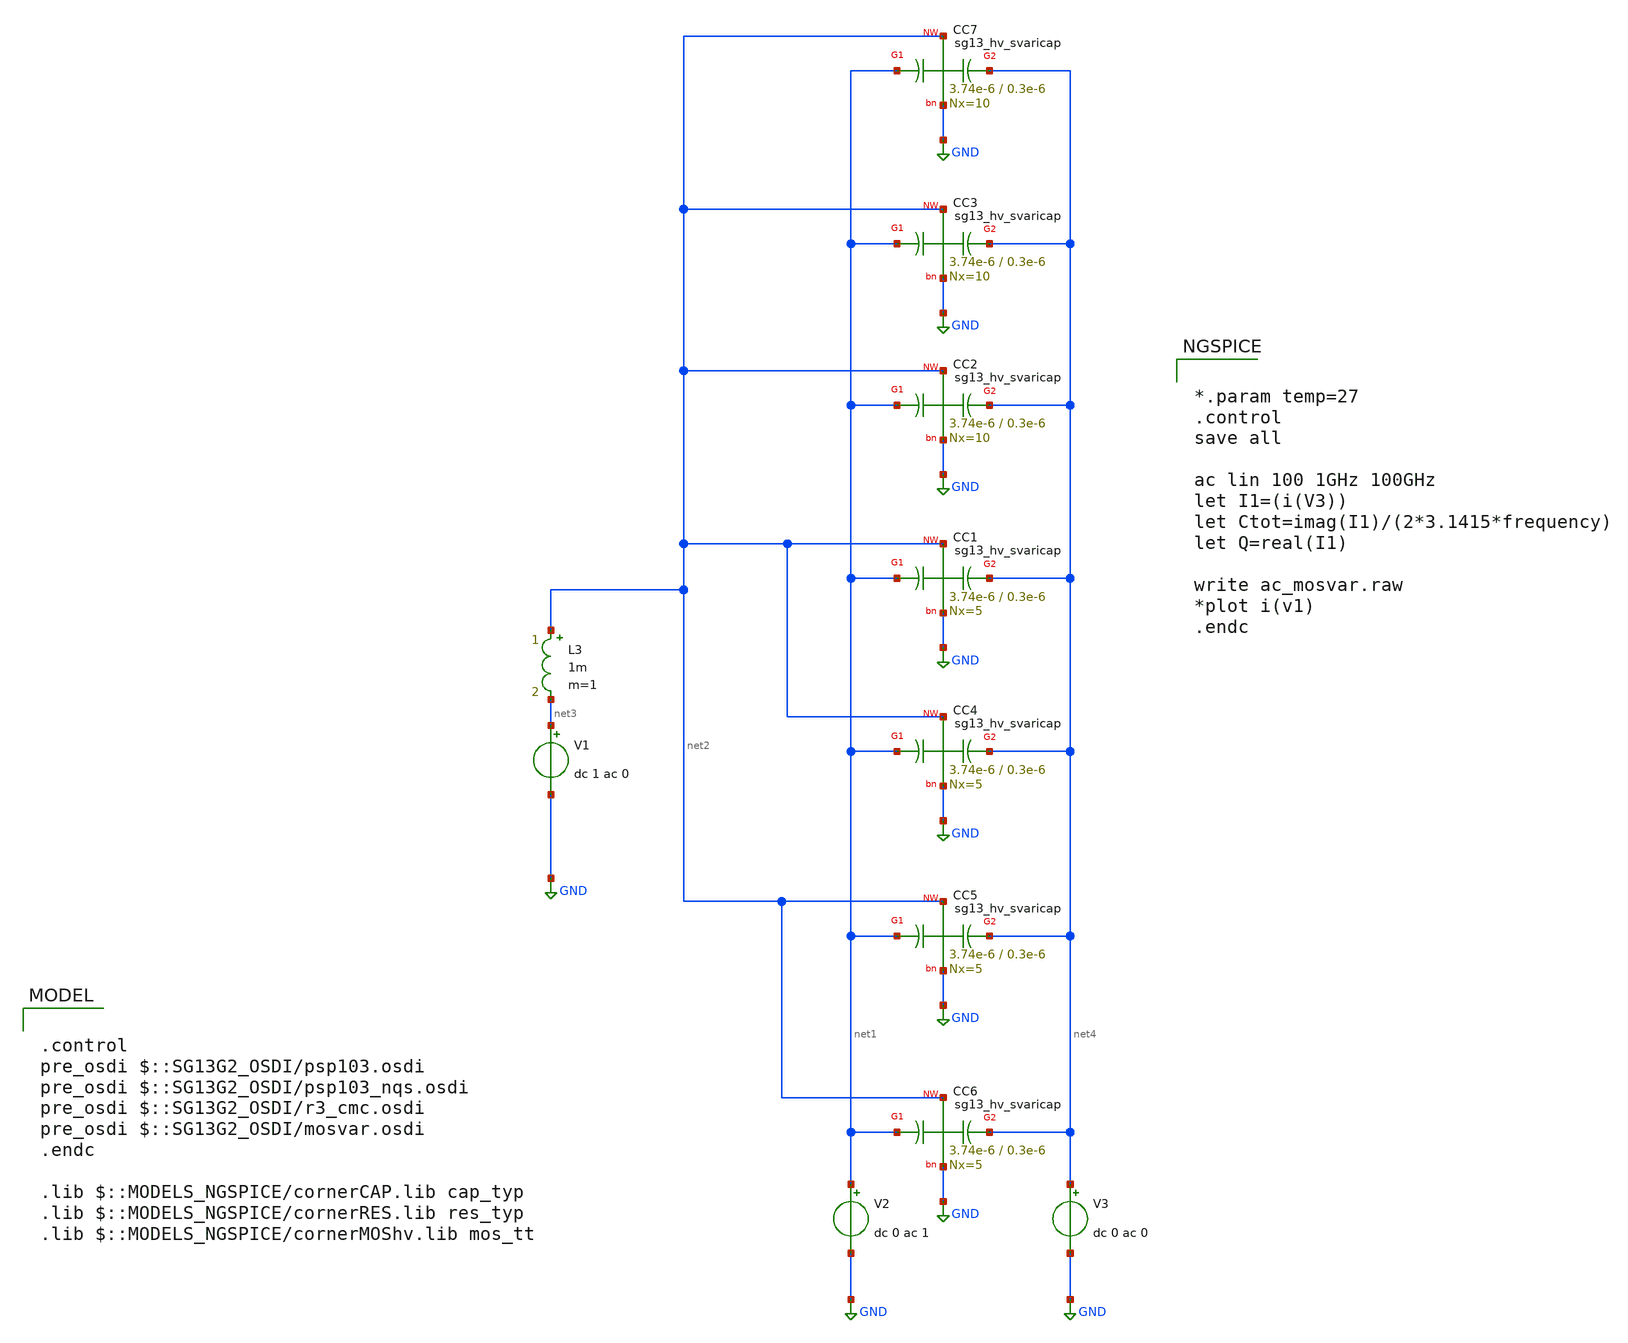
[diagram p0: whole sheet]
** sch_path: ihp-sg13g2/xschem_libs/sg13g2_tests/ac_svaricap_test/schematic/ac_svaricap_test.sch
**.subckt ac_svaricap_test
XC1 net1 net2 net4 GND sg13_hv_svaricap w=3.74e-6 l=0.3e-6 Nx=5
V1 net3 GND dc 1 ac 0
L3 net2 net3 1m m=1
V3 net4 GND dc 0 ac 0
XC2 net1 net2 net4 GND sg13_hv_svaricap w=3.74e-6 l=0.3e-6 Nx=10
XC3 net1 net2 net4 GND sg13_hv_svaricap w=3.74e-6 l=0.3e-6 Nx=10
XC4 net1 net2 net4 GND sg13_hv_svaricap w=3.74e-6 l=0.3e-6 Nx=5
XC5 net1 net2 net4 GND sg13_hv_svaricap w=3.74e-6 l=0.3e-6 Nx=5
XC6 net1 net2 net4 GND sg13_hv_svaricap w=3.74e-6 l=0.3e-6 Nx=5
XC7 net1 net2 net4 GND sg13_hv_svaricap w=3.74e-6 l=0.3e-6 Nx=10
V2 net1 GND dc 0 ac 1
**** begin user architecture code

.control
pre_osdi $::SG13G2_OSDI/psp103.osdi
pre_osdi $::SG13G2_OSDI/psp103_nqs.osdi
pre_osdi $::SG13G2_OSDI/r3_cmc.osdi
pre_osdi $::SG13G2_OSDI/mosvar.osdi
.endc

.lib $::MODELS_NGSPICE/cornerCAP.lib cap_typ
.lib $::MODELS_NGSPICE/cornerRES.lib res_typ
.lib $::MODELS_NGSPICE/cornerMOShv.lib mos_tt



*.param temp=27
.control
save all

ac lin 100 1GHz 100GHz
let I1=(i(V3))
let Ctot=imag(I1)/(2*3.1415*frequency)
let Q=real(I1)

write ac_mosvar.raw
*plot i(v1)
.endc


**** end user architecture code
**.ends
.GLOBAL GND
.end
